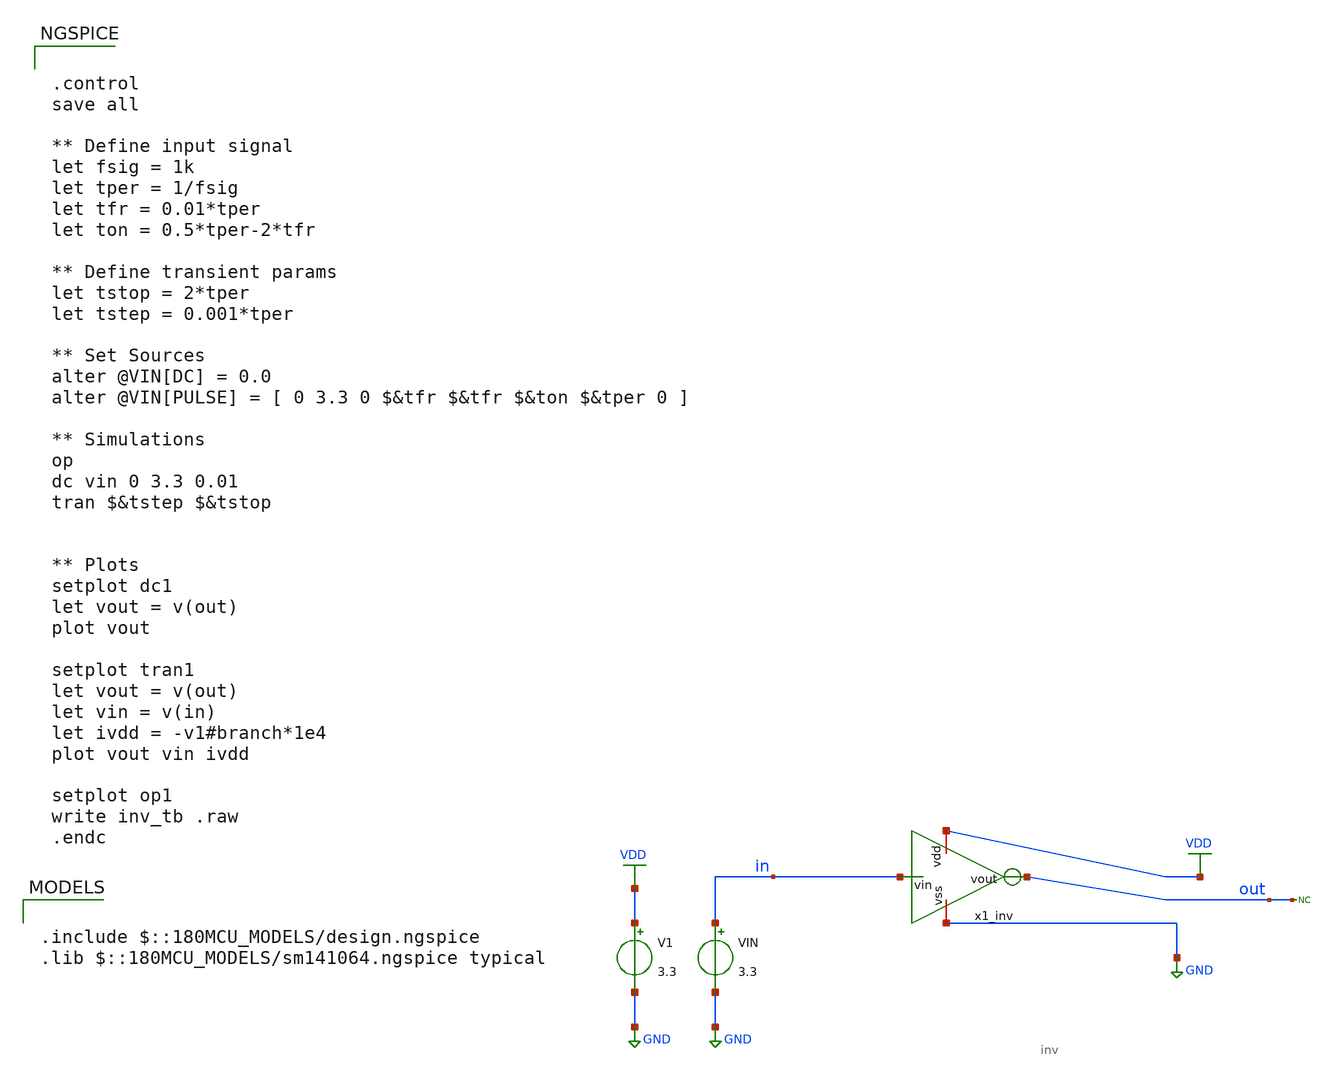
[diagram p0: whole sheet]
** sch_path: designs/inv_tb2.sch
**.subckt inv_tb2
x1_inv VDD in out GND inv
V1 VDD GND 3.3
VIN in GND 3.3
* noconn out
**** begin user architecture code

.include $::180MCU_MODELS/design.ngspice
.lib $::180MCU_MODELS/sm141064.ngspice typical



.control
save all

** Define input signal
let fsig = 1k
let tper = 1/fsig
let tfr = 0.01*tper
let ton = 0.5*tper-2*tfr

** Define transient params
let tstop = 2*tper
let tstep = 0.001*tper

** Set Sources
alter @VIN[DC] = 0.0
alter @VIN[PULSE] = [ 0 3.3 0 $&tfr $&tfr $&ton $&tper 0 ]

** Simulations
op
dc vin 0 3.3 0.01
tran $&tstep $&tstop


** Plots
setplot dc1
let vout = v(out)
plot vout

setplot tran1
let vout = v(out)
let vin = v(in)
let ivdd = -v1#branch*1e4
plot vout vin ivdd

setplot op1
write inv_tb .raw
.endc


**** end user architecture code
**.ends

* expanding   symbol:  inv.sym # of pins=4
** sym_path: designs/inv.sym
** sch_path: designs/inv.sch
.subckt inv vdd vin vout vss
*.iopin vdd
*.iopin vss
*.ipin vin
*.opin vout
XM1 vout vin vdd vdd pfet_03v3 L=0.28u W=0.22u nf=1 ad='int((nf+1)/2) * W/nf * 0.18u' as='int((nf+2)/2) * W/nf * 0.18u'
+ pd='2*int((nf+1)/2) * (W/nf + 0.18u)' ps='2*int((nf+2)/2) * (W/nf + 0.18u)' nrd='0.18u / W' nrs='0.18u / W'
+ sa=0 sb=0 sd=0 m=1
XM2 vout vin vss vss nfet_03v3 L=0.28u W=0.22u nf=1 ad='int((nf+1)/2) * W/nf * 0.18u' as='int((nf+2)/2) * W/nf * 0.18u'
+ pd='2*int((nf+1)/2) * (W/nf + 0.18u)' ps='2*int((nf+2)/2) * (W/nf + 0.18u)' nrd='0.18u / W' nrs='0.18u / W'
+ sa=0 sb=0 sd=0 m=1
.ends

.GLOBAL VDD
.GLOBAL GND
.end
